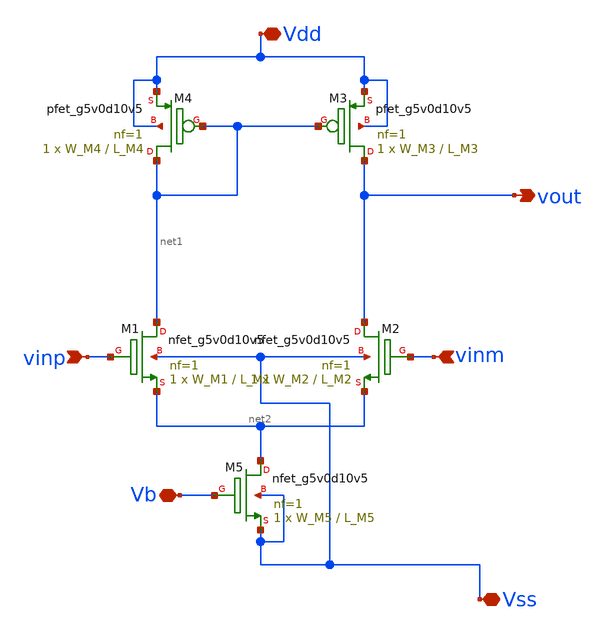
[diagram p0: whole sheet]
** sch_path: xschem/diff_pair.sch
**.subckt diff_pair Vdd vinm vinp Vb vout Vss
*.iopin Vdd
*.ipin vinm
*.ipin vinp
*.iopin Vb
*.opin vout
*.iopin Vss
XM1 net1 vinp net2 Vss sky130_fd_pr__nfet_g5v0d10v5 L=L_M1 W=W_M1 nf=1 ad='int((nf+1)/2) * W/nf * 0.29'
+ as='int((nf+2)/2) * W/nf * 0.29' pd='2*int((nf+1)/2) * (W/nf + 0.29)' ps='2*int((nf+2)/2) * (W/nf + 0.29)'
+ nrd='0.29 / W' nrs='0.29 / W' sa=0 sb=0 sd=0 mult=1 m=1
XM2 vout vinm net2 Vss sky130_fd_pr__nfet_g5v0d10v5 L=L_M2 W=W_M2 nf=1 ad='int((nf+1)/2) * W/nf * 0.29'
+ as='int((nf+2)/2) * W/nf * 0.29' pd='2*int((nf+1)/2) * (W/nf + 0.29)' ps='2*int((nf+2)/2) * (W/nf + 0.29)'
+ nrd='0.29 / W' nrs='0.29 / W' sa=0 sb=0 sd=0 mult=1 m=1
XM3 vout net1 Vdd Vdd sky130_fd_pr__pfet_g5v0d10v5 L=L_M3 W=W_M3 nf=1 ad='int((nf+1)/2) * W/nf * 0.29'
+ as='int((nf+2)/2) * W/nf * 0.29' pd='2*int((nf+1)/2) * (W/nf + 0.29)' ps='2*int((nf+2)/2) * (W/nf + 0.29)'
+ nrd='0.29 / W' nrs='0.29 / W' sa=0 sb=0 sd=0 mult=1 m=1
XM4 net1 net1 Vdd Vdd sky130_fd_pr__pfet_g5v0d10v5 L=L_M4 W=W_M4 nf=1 ad='int((nf+1)/2) * W/nf * 0.29'
+ as='int((nf+2)/2) * W/nf * 0.29' pd='2*int((nf+1)/2) * (W/nf + 0.29)' ps='2*int((nf+2)/2) * (W/nf + 0.29)'
+ nrd='0.29 / W' nrs='0.29 / W' sa=0 sb=0 sd=0 mult=1 m=1
XM5 net2 Vb Vss Vss sky130_fd_pr__nfet_g5v0d10v5 L=L_M5 W=W_M5 nf=1 ad='int((nf+1)/2) * W/nf * 0.29'
+ as='int((nf+2)/2) * W/nf * 0.29' pd='2*int((nf+1)/2) * (W/nf + 0.29)' ps='2*int((nf+2)/2) * (W/nf + 0.29)'
+ nrd='0.29 / W' nrs='0.29 / W' sa=0 sb=0 sd=0 mult=1 m=1
**.ends
.end
